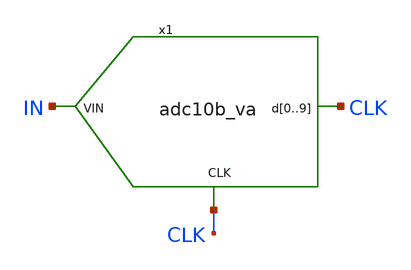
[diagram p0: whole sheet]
** sch_path: xschem/signal_test.sch
.lib $::SKYWATER_MODELS/sky130.lib.spice tt
.include $::SKYWATER_STDCELLS/sky130_fd_sc_hd.spice

**.subckt signal_test
x1 IN CLK CLK CLK CLK CLK CLK CLK CLK CLK CLK CLK adc10b_va
**** begin user architecture code



  *.options wnflag=0 bypass=1
  .option wnflag=1
  .option safecurrents
  *.option klu
  .options solver=klu nomod
  .options method=gear rawfile=binary
  .options reltol=1e-2
  ********************Static Voltage Sources***************************
  Vddh vddh gnd dc 5.5
  Vdd vdd gnd dc 1.8
  Vdda vdda gnd dc 5.5
  Vgnda gnda gnd dc 0

  *Vin in gnd 5

  VHREF x1.V[191] GND 5.5
  VLREF x1.V[0] GND 0
  *****INPUT SIGNALS******
  .param LSB0 = {1024/(2**10)}
  .param LSB1 = {1.8/(2**9)}
  .param LSB2 = {1.8/(2**8)}
  .param LSB3 = {1.8/(2**7)}
  .param LSB4 = {1.8/(2**6)}
  .param LSB5 = {1.8/(2**5)}
  .param LSB6 = {1.8/(2**4)}
  .param LSB7 = {1.8/(2**3)}
  .param LSB8 = {1.8/(2**2)}
  .param LSB9 = {1.8/(2**1)}

  Bd0  d[0]  gnd V = {V(in) - 2*LSB0*floor(V(in)/(2*LSB0)) >= 1*LSB0 ? 1.8 : 0}
  Bd1  d[1]  gnd V = {V(in) - 4*LSB0*floor(V(in)/(4*LSB0)) >= 2*LSB0 ? 1.8 : 0}
  Bd2  d[2]  gnd V = {V(in) - 8*LSB0*floor(V(in)/(8*LSB0)) >= 4*LSB0 ? 1.8 : 0}
  Bd3  d[3]  gnd V = {V(in) - 16*LSB0*floor(V(in)/(16*LSB0)) >= 8*LSB0 ? 1.8 : 0}
  Bd4  d[4]  gnd V = {V(in) - 32*LSB0*floor(V(in)/(32*LSB0)) >= 16*LSB0 ? 1.8 : 0}
  Bd5  d[5]  gnd V = {V(in) - 64*LSB0*floor(V(in)/(64*LSB0)) >= 32*LSB0 ? 1.8 : 0}
  Bd6  d[6]  gnd V = {V(in) - 128*LSB0*floor(V(in)/(128*LSB0)) >= 64*LSB0 ? 1.8 : 0}
  Bd7  d[7]  gnd V = {V(in) - 256*LSB0*floor(V(in)/(256*LSB0)) >= 128*LSB0 ? 1.8 : 0}
  Bd8  d[8]  gnd V = {V(in) - 512*LSB0*floor(V(in)/(512*LSB0)) >= 256*LSB0 ? 1.8 : 0}
  Bd9  d[9]  gnd V = {V(in) - 1024*LSB0*floor(V(in)/(1024*LSB0)) >= 512*LSB0 ? 1.8 : 0}


  Vin in gnd SIN(512 512 9.95k)
  Vclk clk gnd pulse(1.8 0 10n 10n 0 5u 10u)

  .subckt adc10b_va in clk d0 d1 d2 d3 d4 d5 d6 d7 d8 d9
  N1 in clk d0 d1 d2 d3 d4 d5 d6 d7 d8 d9 adc_model
  .ends
  .model adc_model adc10bit
  ********************Simulation Commands*****************************
  .control
     reset
     set num_threads=36
     option numdgt=6
     set wr_singlescale
     set wr_vecnames
     *dc vin 0 1.8 0.0017578125
     dc vin 0 1024 1
     *tran 10n 1m

     *let vval = V(in)
     *let testvar = {floor(vval*1024/1.8)}

     save all
     *save testvar
     write signal_test-tb.raw
     *&write signal_test_dc-tb.raw

*    quit 0
  .endc



**** end user architecture code
**.ends
.end
